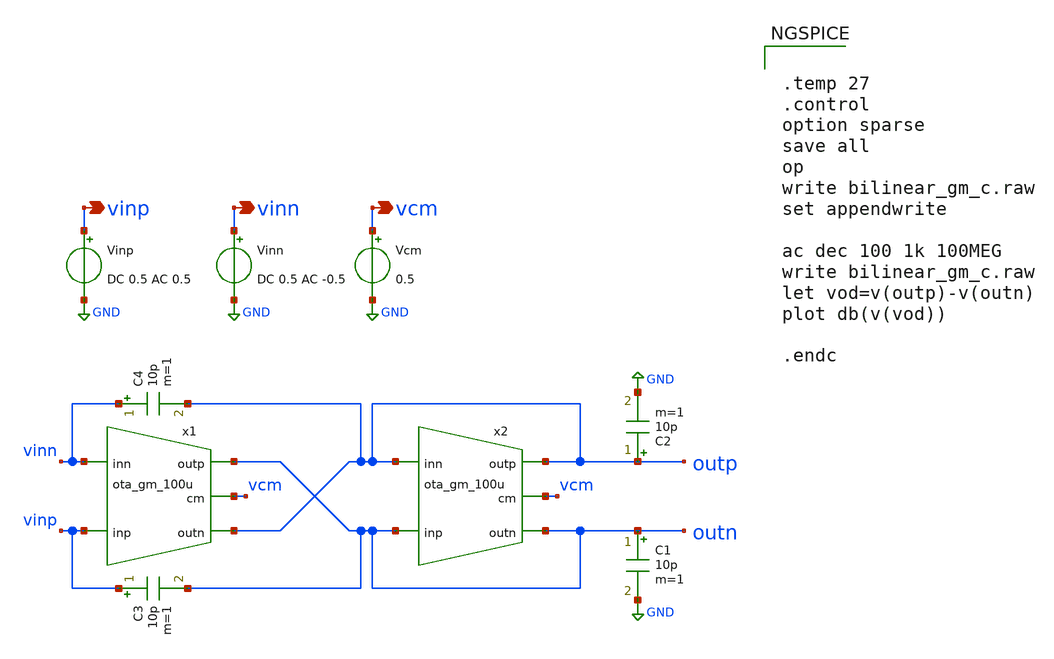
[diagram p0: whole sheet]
** sch_path: prj/template/2_Idealized_circuits/bilinear_gm_c.sch
**.subckt bilinear_gm_c vinp vinn vcm
*.opin vinp
*.opin vinn
*.opin vcm
x1 vinp vinn outn outp vcm ota_gm_100u
x2 outn outp outp outn vcm ota_gm_100u
C1 outn GND 10p m=1
Vinp vinp GND DC 0.5 AC 0.5
Vinn vinn GND DC 0.5 AC -0.5
Vcm vcm GND 0.5
C2 outp GND 10p m=1
C3 vinp outn 10p m=1
C4 vinn outp 10p m=1
**** begin user architecture code


.temp 27
.control
option sparse
save all
op
write bilinear_gm_c.raw
set appendwrite

ac dec 100 1k 100MEG
write bilinear_gm_c.raw
let vod=v(outp)-v(outn)
plot db(v(vod))

.endc


**** end user architecture code
**.ends
.GLOBAL GND
.end
